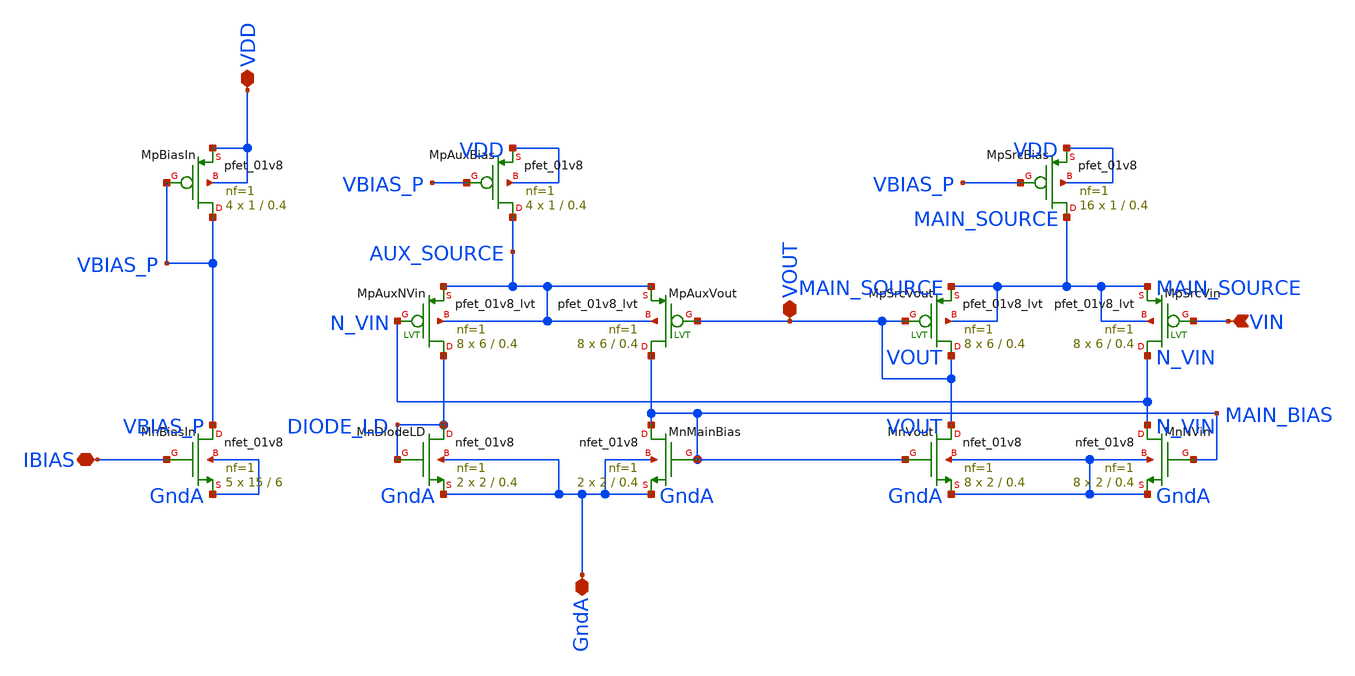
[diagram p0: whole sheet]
** sch_path: analog/xschem/infiniamp_xl.sch
**.subckt infiniamp_xl VDD GndA VIN IBIAS VOUT
*.iopin VDD
*.iopin GndA
*.ipin VIN
*.iopin IBIAS
*.iopin VOUT
XMpBiasIn VBIAS_P VBIAS_P VDD VDD sky130_fd_pr__pfet_01v8 L=0.4 W=1 nf=1 ad='int((1 + 1)/2) * 1 / 1 * 0.29'
+ as='int((1 + 2)/2) * 1 / 1 * 0.29' pd='2*int((1 + 1)/2) * (1 / 1 + 0.29)' ps='2*int((1 + 2)/2) * (1 / 1 + 0.29)'
+ nrd='0.29 / 1 ' nrs='0.29 / 1 ' sa=0 sb=0 sd=0 mult=4 m=4
XMpAuxBias AUX_SOURCE VBIAS_P VDD VDD sky130_fd_pr__pfet_01v8 L=0.4 W=1 nf=1 ad='int((1 + 1)/2) * 1 / 1 * 0.29'
+ as='int((1 + 2)/2) * 1 / 1 * 0.29' pd='2*int((1 + 1)/2) * (1 / 1 + 0.29)' ps='2*int((1 + 2)/2) * (1 / 1 + 0.29)'
+ nrd='0.29 / 1 ' nrs='0.29 / 1 ' sa=0 sb=0 sd=0 mult=4 m=4
XMpSrcBias MAIN_SOURCE VBIAS_P VDD VDD sky130_fd_pr__pfet_01v8 L=0.4 W=1 nf=1 ad='int((1 + 1)/2) * 1 / 1 * 0.29'
+ as='int((1 + 2)/2) * 1 / 1 * 0.29' pd='2*int((1 + 1)/2) * (1 / 1 + 0.29)' ps='2*int((1 + 2)/2) * (1 / 1 + 0.29)'
+ nrd='0.29 / 1 ' nrs='0.29 / 1 ' sa=0 sb=0 sd=0 mult=16 m=16
XMpAuxNVin DIODE_LD N_VIN AUX_SOURCE AUX_SOURCE sky130_fd_pr__pfet_01v8_lvt L=0.4 W=6 nf=1 ad='int((1 + 1)/2) * 6 / 1 * 0.29'
+ as='int((1 + 2)/2) * 6 / 1 * 0.29' pd='2*int((1 + 1)/2) * (6 / 1 + 0.29)' ps='2*int((1 + 2)/2) * (6 / 1 + 0.29)'
+ nrd='0.29 / 6 ' nrs='0.29 / 6 ' sa=0 sb=0 sd=0 mult=8 m=8
XMpAuxVout MAIN_BIAS VOUT AUX_SOURCE AUX_SOURCE sky130_fd_pr__pfet_01v8_lvt L=0.4 W=6 nf=1 ad='int((1 + 1)/2) * 6 / 1 * 0.29'
+ as='int((1 + 2)/2) * 6 / 1 * 0.29' pd='2*int((1 + 1)/2) * (6 / 1 + 0.29)' ps='2*int((1 + 2)/2) * (6 / 1 + 0.29)'
+ nrd='0.29 / 6 ' nrs='0.29 / 6 ' sa=0 sb=0 sd=0 mult=8 m=8
XMpSrcVin N_VIN VIN MAIN_SOURCE MAIN_SOURCE sky130_fd_pr__pfet_01v8_lvt L=0.4 W=6 nf=1 ad='int((1 + 1)/2) * 6 / 1 * 0.29'
+ as='int((1 + 2)/2) * 6 / 1 * 0.29' pd='2*int((1 + 1)/2) * (6 / 1 + 0.29)' ps='2*int((1 + 2)/2) * (6 / 1 + 0.29)'
+ nrd='0.29 / 6 ' nrs='0.29 / 6 ' sa=0 sb=0 sd=0 mult=8 m=8
XMpSrcVout VOUT VOUT MAIN_SOURCE MAIN_SOURCE sky130_fd_pr__pfet_01v8_lvt L=0.4 W=6 nf=1 ad='int((1 + 1)/2) * 6 / 1 * 0.29'
+ as='int((1 + 2)/2) * 6 / 1 * 0.29' pd='2*int((1 + 1)/2) * (6 / 1 + 0.29)' ps='2*int((1 + 2)/2) * (6 / 1 + 0.29)'
+ nrd='0.29 / 6 ' nrs='0.29 / 6 ' sa=0 sb=0 sd=0 mult=8 m=8
XMnBiasIn VBIAS_P IBIAS GndA GndA sky130_fd_pr__nfet_01v8 L=6 W=15 nf=1 ad='int((1 + 1)/2) * 15 / 1 * 0.29'
+ as='int((1 + 2)/2) * 15 / 1 * 0.29' pd='2*int((1 + 1)/2) * (15 / 1 + 0.29)' ps='2*int((1 + 2)/2) * (15 / 1 + 0.29)'
+ nrd='0.29 / 15 ' nrs='0.29 / 15 ' sa=0 sb=0 sd=0 mult=5 m=5
XMnDiodeLD DIODE_LD DIODE_LD GndA GndA sky130_fd_pr__nfet_01v8 L=0.4 W=2 nf=1 ad='int((1 + 1)/2) * 2 / 1 * 0.29'
+ as='int((1 + 2)/2) * 2 / 1 * 0.29' pd='2*int((1 + 1)/2) * (2 / 1 + 0.29)' ps='2*int((1 + 2)/2) * (2 / 1 + 0.29)'
+ nrd='0.29 / 2 ' nrs='0.29 / 2 ' sa=0 sb=0 sd=0 mult=2 m=2
XMnMainBias MAIN_BIAS MAIN_BIAS GndA GndA sky130_fd_pr__nfet_01v8 L=0.4 W=2 nf=1 ad='int((1 + 1)/2) * 2 / 1 * 0.29'
+ as='int((1 + 2)/2) * 2 / 1 * 0.29' pd='2*int((1 + 1)/2) * (2 / 1 + 0.29)' ps='2*int((1 + 2)/2) * (2 / 1 + 0.29)'
+ nrd='0.29 / 2 ' nrs='0.29 / 2 ' sa=0 sb=0 sd=0 mult=2 m=2
XMnNVin N_VIN MAIN_BIAS GndA GndA sky130_fd_pr__nfet_01v8 L=0.4 W=2 nf=1 ad='int((1 + 1)/2) * 2 / 1 * 0.29'
+ as='int((1 + 2)/2) * 2 / 1 * 0.29' pd='2*int((1 + 1)/2) * (2 / 1 + 0.29)' ps='2*int((1 + 2)/2) * (2 / 1 + 0.29)'
+ nrd='0.29 / 2 ' nrs='0.29 / 2 ' sa=0 sb=0 sd=0 mult=8 m=8
XMnVout VOUT MAIN_BIAS GndA GndA sky130_fd_pr__nfet_01v8 L=0.4 W=2 nf=1 ad='int((1 + 1)/2) * 2 / 1 * 0.29'
+ as='int((1 + 2)/2) * 2 / 1 * 0.29' pd='2*int((1 + 1)/2) * (2 / 1 + 0.29)' ps='2*int((1 + 2)/2) * (2 / 1 + 0.29)'
+ nrd='0.29 / 2 ' nrs='0.29 / 2 ' sa=0 sb=0 sd=0 mult=8 m=8
**.ends
.end
